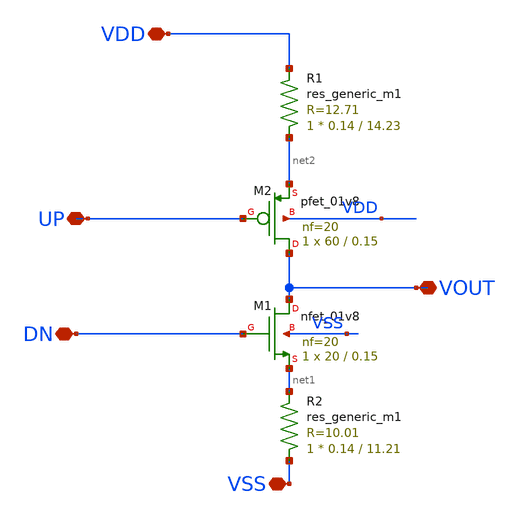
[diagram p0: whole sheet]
** sch_path: xschem/DC_DC_Converter_xschem/DC_DC_Converter/current_pump/current_pump_for_symbol.sch
**.subckt current_pump_for_symbol VDD UP DN VSS VOUT
*.iopin VDD
*.iopin UP
*.iopin DN
*.iopin VSS
*.iopin VOUT
XM1 VOUT DN net1 VSS sky130_fd_pr__nfet_01v8 L=0.15 W=20 nf=20 ad='int((nf+1)/2) * W/nf * 0.29' as='int((nf+2)/2) * W/nf * 0.29'
+ pd='2*int((nf+1)/2) * (W/nf + 0.29)' ps='2*int((nf+2)/2) * (W/nf + 0.29)' nrd='0.29 / W' nrs='0.29 / W'
+ sa=0 sb=0 sd=0 mult=1 m=1
XM2 VOUT UP net2 VDD sky130_fd_pr__pfet_01v8 L=0.15 W=60 nf=20 ad='int((nf+1)/2) * W/nf * 0.29' as='int((nf+2)/2) * W/nf * 0.29'
+ pd='2*int((nf+1)/2) * (W/nf + 0.29)' ps='2*int((nf+2)/2) * (W/nf + 0.29)' nrd='0.29 / W' nrs='0.29 / W'
+ sa=0 sb=0 sd=0 mult=1 m=1
R1 net2 VDD sky130_fd_pr__res_generic_m1 W=0.14 L=14.23 m=1
R2 VSS net1 sky130_fd_pr__res_generic_m1 W=0.14 L=11.21 m=1
**.ends
.end
